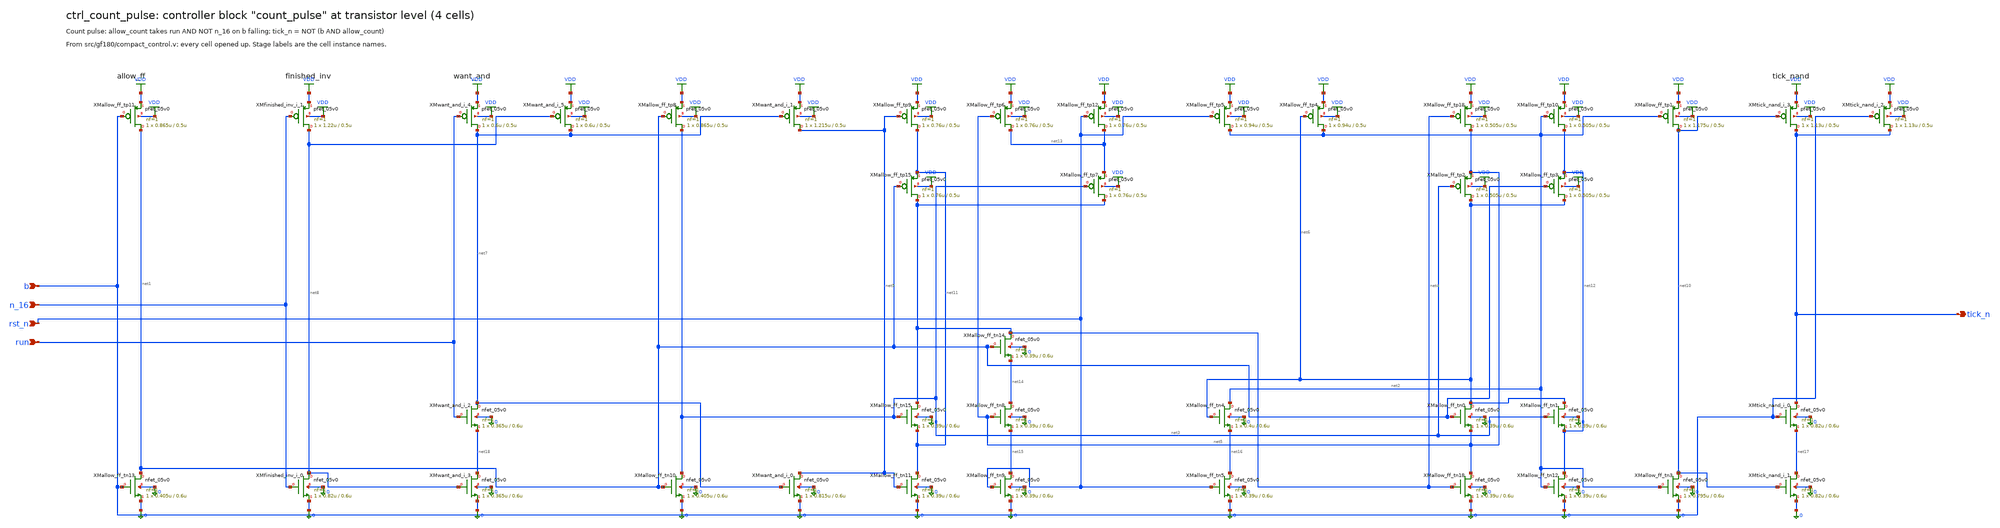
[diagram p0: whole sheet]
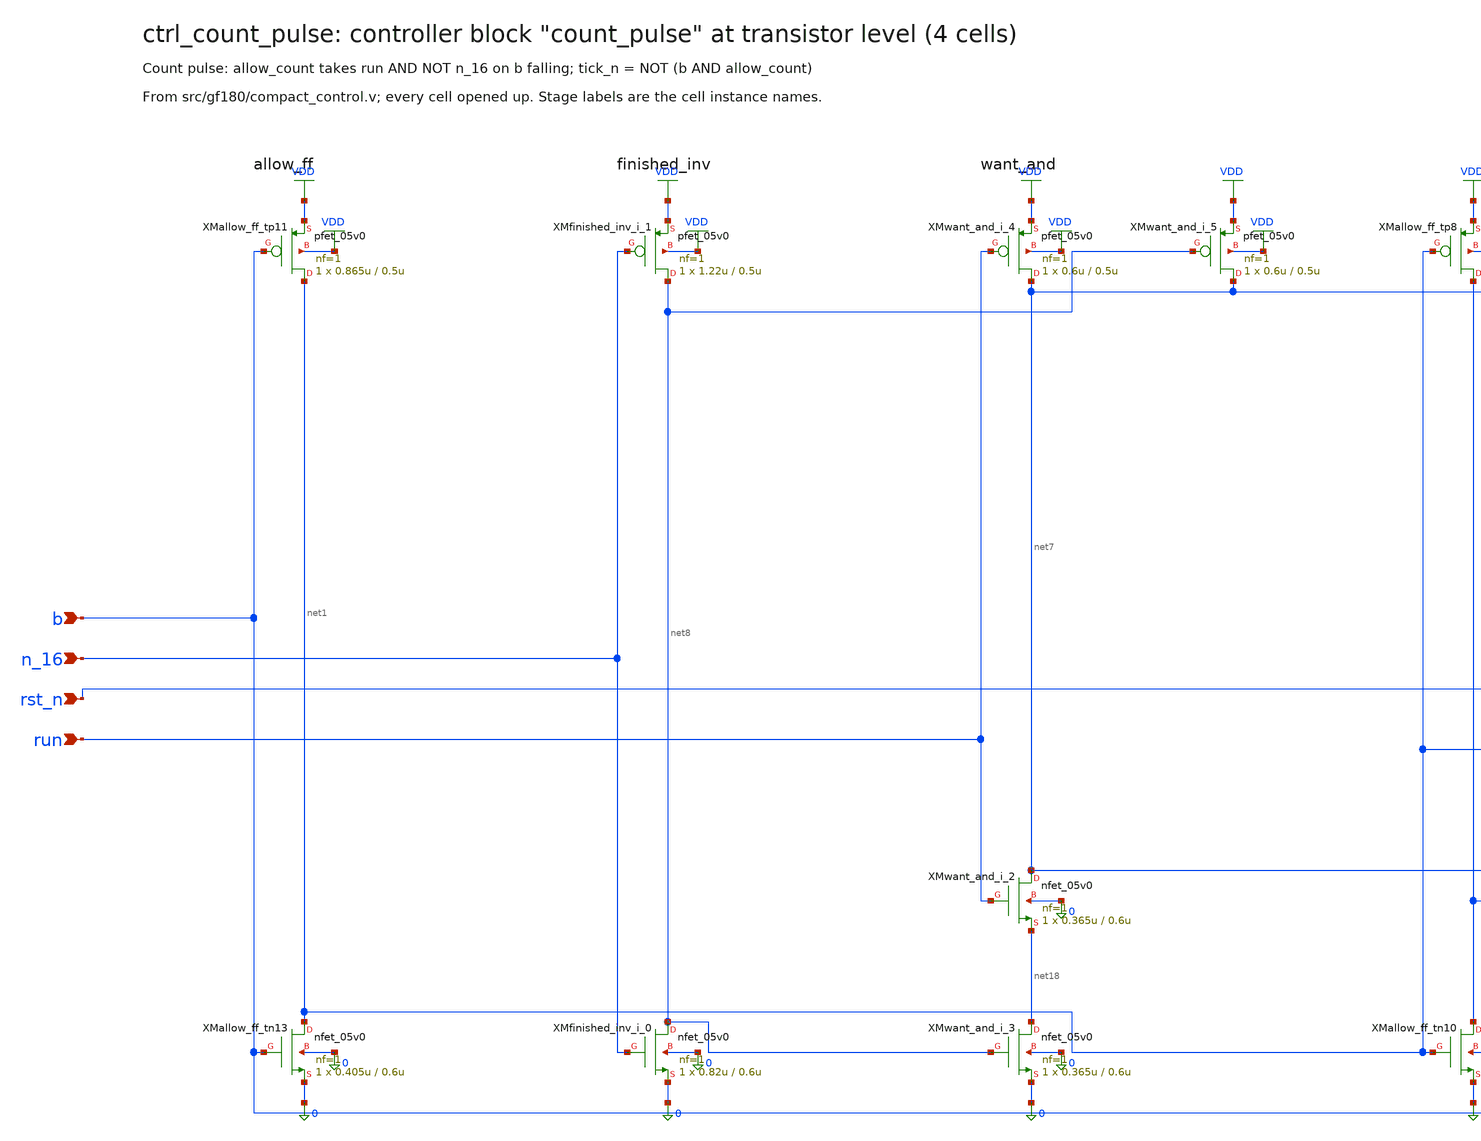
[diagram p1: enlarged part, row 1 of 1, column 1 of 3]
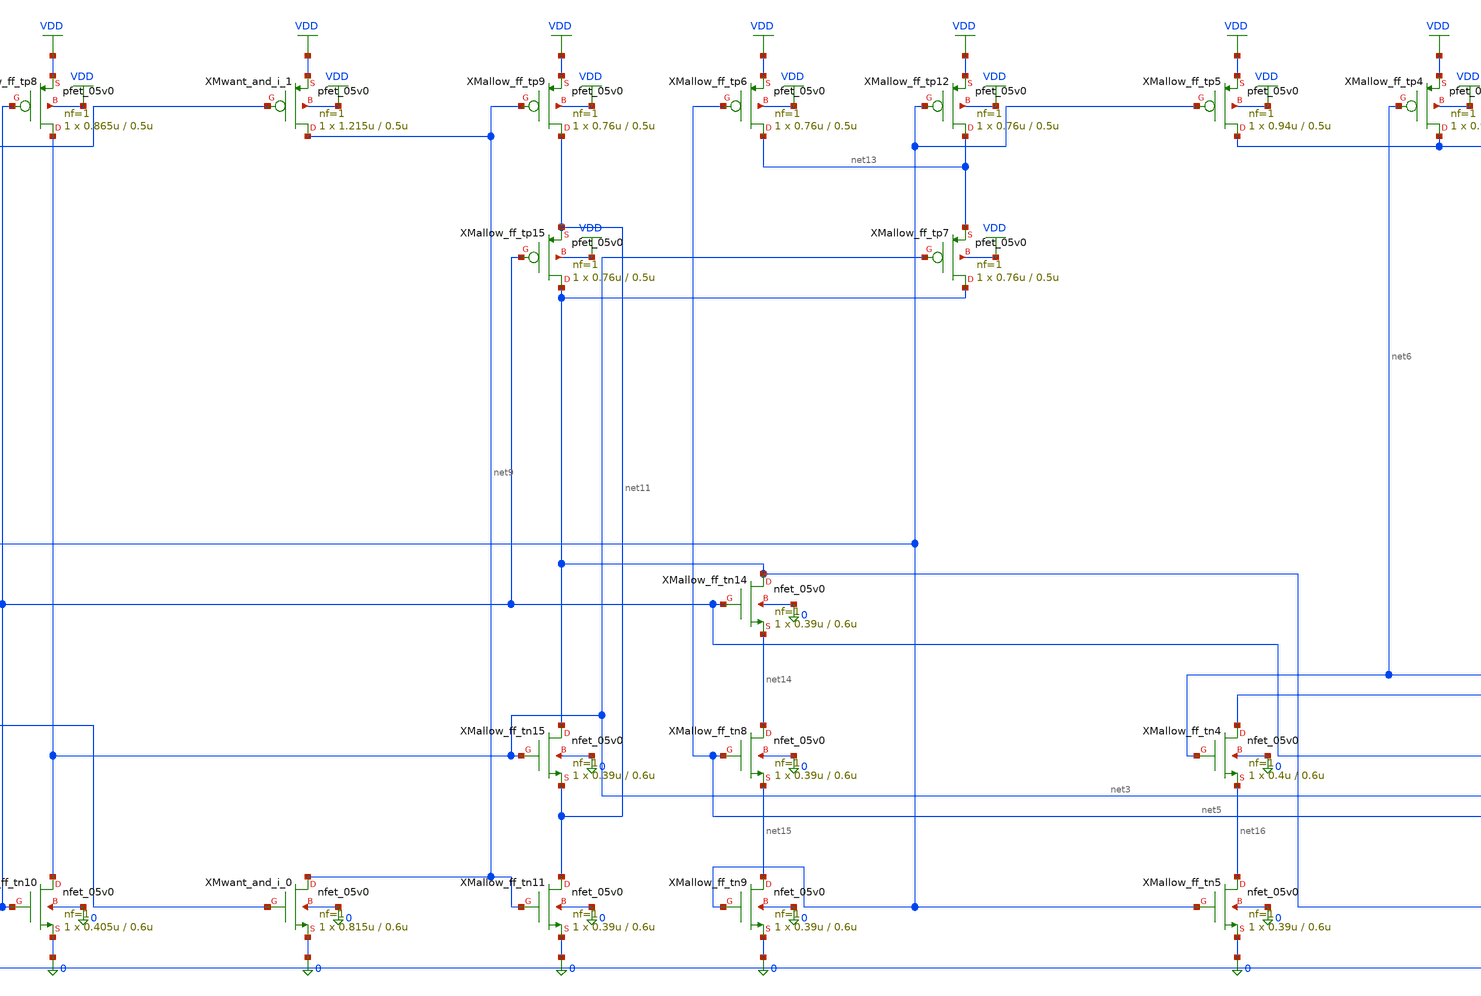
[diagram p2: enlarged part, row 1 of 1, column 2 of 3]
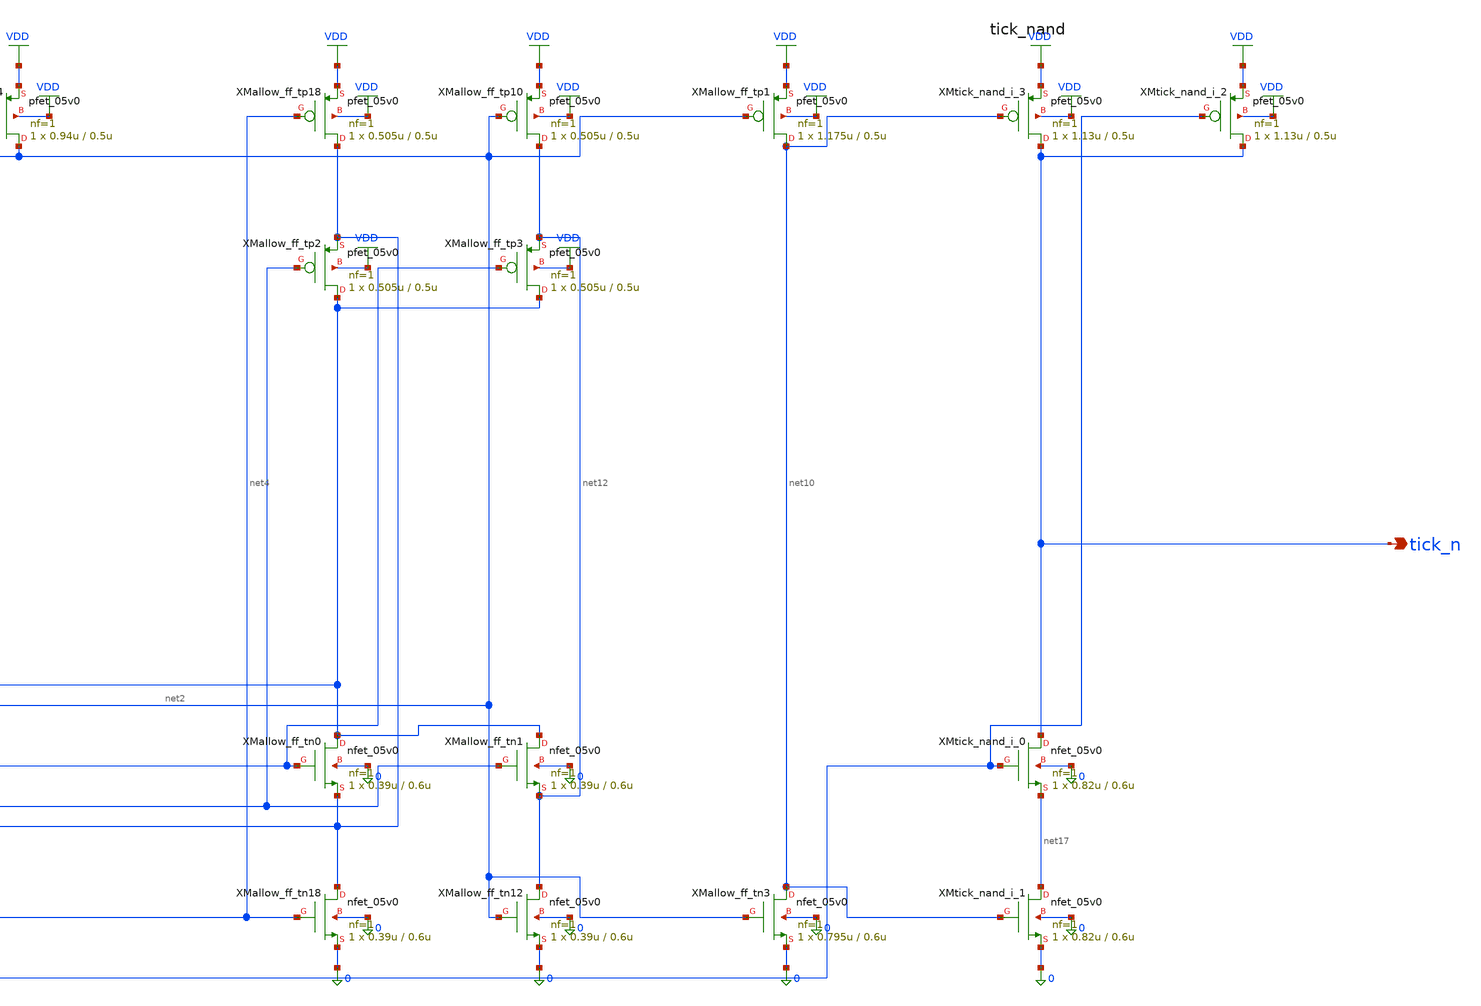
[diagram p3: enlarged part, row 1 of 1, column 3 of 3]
** sch_path: xschem/flat/ctrl_count_pulse.sch
**.subckt ctrl_count_pulse b n_16 rst_n run tick_n
*.ipin b
*.ipin n_16
*.ipin rst_n
*.ipin run
*.opin tick_n
XMallow_ff_tn13 net1 b 0 0 nfet_05v0 L=0.6u W=0.405u nf=1 ad=2.025e-13 as=2.025e-13 pd=1.81e-06
+ ps=1.81e-06 nrd=0 nrs=0 sa=0 sb=0 sd=0 m=1
XMallow_ff_tn10 net3 net1 0 0 nfet_05v0 L=0.6u W=0.405u nf=1 ad=2.025e-13 as=2.025e-13 pd=1.81e-06
+ ps=1.81e-06 nrd=0 nrs=0 sa=0 sb=0 sd=0 m=1
XMallow_ff_tn11 net11 net9 0 0 nfet_05v0 L=0.6u W=0.39u nf=1 ad=1.95e-13 as=1.95e-13 pd=1.78e-06
+ ps=1.78e-06 nrd=0 nrs=0 sa=0 sb=0 sd=0 m=1
XMallow_ff_tn15 net4 net3 net11 0 nfet_05v0 L=0.6u W=0.39u nf=1 ad=1.95e-13 as=1.95e-13 pd=1.78e-06
+ ps=1.78e-06 nrd=0 nrs=0 sa=0 sb=0 sd=0 m=1
XMallow_ff_tn14 net4 net1 net14 0 nfet_05v0 L=0.6u W=0.39u nf=1 ad=1.95e-13 as=1.95e-13 pd=1.78e-06
+ ps=1.78e-06 nrd=0 nrs=0 sa=0 sb=0 sd=0 m=1
XMallow_ff_tn8 net14 net5 net15 0 nfet_05v0 L=0.6u W=0.39u nf=1 ad=1.95e-13 as=1.95e-13 pd=1.78e-06
+ ps=1.78e-06 nrd=0 nrs=0 sa=0 sb=0 sd=0 m=1
XMallow_ff_tn9 net15 rst_n 0 0 nfet_05v0 L=0.6u W=0.39u nf=1 ad=1.95e-13 as=1.95e-13 pd=1.78e-06
+ ps=1.78e-06 nrd=0 nrs=0 sa=0 sb=0 sd=0 m=1
XMallow_ff_tn18 net5 net4 0 0 nfet_05v0 L=0.6u W=0.39u nf=1 ad=1.95e-13 as=1.95e-13 pd=1.78e-06
+ ps=1.78e-06 nrd=0 nrs=0 sa=0 sb=0 sd=0 m=1
XMallow_ff_tn0 net6 net1 net5 0 nfet_05v0 L=0.6u W=0.39u nf=1 ad=1.95e-13 as=1.95e-13 pd=1.78e-06
+ ps=1.78e-06 nrd=0 nrs=0 sa=0 sb=0 sd=0 m=1
XMallow_ff_tn1 net6 net3 net12 0 nfet_05v0 L=0.6u W=0.39u nf=1 ad=1.95e-13 as=1.95e-13 pd=1.78e-06
+ ps=1.78e-06 nrd=0 nrs=0 sa=0 sb=0 sd=0 m=1
XMallow_ff_tn12 net12 net2 0 0 nfet_05v0 L=0.6u W=0.39u nf=1 ad=1.95e-13 as=1.95e-13 pd=1.78e-06
+ ps=1.78e-06 nrd=0 nrs=0 sa=0 sb=0 sd=0 m=1
XMallow_ff_tn5 net16 rst_n 0 0 nfet_05v0 L=0.6u W=0.39u nf=1 ad=1.95e-13 as=1.95e-13 pd=1.78e-06
+ ps=1.78e-06 nrd=0 nrs=0 sa=0 sb=0 sd=0 m=1
XMallow_ff_tn4 net2 net6 net16 0 nfet_05v0 L=0.6u W=0.4u nf=1 ad=2e-13 as=2e-13 pd=1.8e-06
+ ps=1.8e-06 nrd=0 nrs=0 sa=0 sb=0 sd=0 m=1
XMallow_ff_tn3 net10 net2 0 0 nfet_05v0 L=0.6u W=0.795u nf=1 ad=3.975e-13 as=3.975e-13 pd=2.59e-06
+ ps=2.59e-06 nrd=0 nrs=0 sa=0 sb=0 sd=0 m=1
XMallow_ff_tp11 net1 b VDD VDD pfet_05v0 L=0.5u W=0.865u nf=1 ad=4.325e-13 as=4.325e-13 pd=2.73e-06
+ ps=2.73e-06 nrd=0 nrs=0 sa=0 sb=0 sd=0 m=1
XMallow_ff_tp8 net3 net1 VDD VDD pfet_05v0 L=0.5u W=0.865u nf=1 ad=4.325e-13 as=4.325e-13
+ pd=2.73e-06 ps=2.73e-06 nrd=0 nrs=0 sa=0 sb=0 sd=0 m=1
XMallow_ff_tp9 net11 net9 VDD VDD pfet_05v0 L=0.5u W=0.76u nf=1 ad=3.8e-13 as=3.8e-13 pd=2.52e-06
+ ps=2.52e-06 nrd=0 nrs=0 sa=0 sb=0 sd=0 m=1
XMallow_ff_tp15 net4 net1 net11 VDD pfet_05v0 L=0.5u W=0.76u nf=1 ad=3.8e-13 as=3.8e-13 pd=2.52e-06
+ ps=2.52e-06 nrd=0 nrs=0 sa=0 sb=0 sd=0 m=1
XMallow_ff_tp7 net4 net3 net13 VDD pfet_05v0 L=0.5u W=0.76u nf=1 ad=3.8e-13 as=3.8e-13 pd=2.52e-06
+ ps=2.52e-06 nrd=0 nrs=0 sa=0 sb=0 sd=0 m=1
XMallow_ff_tp6 net13 net5 VDD VDD pfet_05v0 L=0.5u W=0.76u nf=1 ad=3.8e-13 as=3.8e-13 pd=2.52e-06
+ ps=2.52e-06 nrd=0 nrs=0 sa=0 sb=0 sd=0 m=1
XMallow_ff_tp12 net13 rst_n VDD VDD pfet_05v0 L=0.5u W=0.76u nf=1 ad=3.8e-13 as=3.8e-13 pd=2.52e-06
+ ps=2.52e-06 nrd=0 nrs=0 sa=0 sb=0 sd=0 m=1
XMallow_ff_tp18 net5 net4 VDD VDD pfet_05v0 L=0.5u W=0.505u nf=1 ad=2.525e-13 as=2.525e-13
+ pd=2.01e-06 ps=2.01e-06 nrd=0 nrs=0 sa=0 sb=0 sd=0 m=1
XMallow_ff_tp2 net6 net3 net5 VDD pfet_05v0 L=0.5u W=0.505u nf=1 ad=2.525e-13 as=2.525e-13
+ pd=2.01e-06 ps=2.01e-06 nrd=0 nrs=0 sa=0 sb=0 sd=0 m=1
XMallow_ff_tp3 net6 net1 net12 VDD pfet_05v0 L=0.5u W=0.505u nf=1 ad=2.525e-13 as=2.525e-13
+ pd=2.01e-06 ps=2.01e-06 nrd=0 nrs=0 sa=0 sb=0 sd=0 m=1
XMallow_ff_tp10 net12 net2 VDD VDD pfet_05v0 L=0.5u W=0.505u nf=1 ad=2.525e-13 as=2.525e-13
+ pd=2.01e-06 ps=2.01e-06 nrd=0 nrs=0 sa=0 sb=0 sd=0 m=1
XMallow_ff_tp5 net2 rst_n VDD VDD pfet_05v0 L=0.5u W=0.94u nf=1 ad=4.7e-13 as=4.7e-13 pd=2.88e-06
+ ps=2.88e-06 nrd=0 nrs=0 sa=0 sb=0 sd=0 m=1
XMallow_ff_tp4 net2 net6 VDD VDD pfet_05v0 L=0.5u W=0.94u nf=1 ad=4.7e-13 as=4.7e-13 pd=2.88e-06
+ ps=2.88e-06 nrd=0 nrs=0 sa=0 sb=0 sd=0 m=1
XMallow_ff_tp1 net10 net2 VDD VDD pfet_05v0 L=0.5u W=1.175u nf=1 ad=5.875e-13 as=5.875e-13
+ pd=3.35e-06 ps=3.35e-06 nrd=0 nrs=0 sa=0 sb=0 sd=0 m=1
XMfinished_inv_i_0 net8 n_16 0 0 nfet_05v0 L=0.6u W=0.82u nf=1 ad=4.1e-13 as=4.1e-13 pd=2.64e-06
+ ps=2.64e-06 nrd=0 nrs=0 sa=0 sb=0 sd=0 m=1
XMfinished_inv_i_1 net8 n_16 VDD VDD pfet_05v0 L=0.5u W=1.22u nf=1 ad=6.1e-13 as=6.1e-13 pd=3.44e-06
+ ps=3.44e-06 nrd=0 nrs=0 sa=0 sb=0 sd=0 m=1
XMtick_nand_i_1 net17 net10 0 0 nfet_05v0 L=0.6u W=0.82u nf=1 ad=4.1e-13 as=4.1e-13 pd=2.64e-06
+ ps=2.64e-06 nrd=0 nrs=0 sa=0 sb=0 sd=0 m=1
XMtick_nand_i_0 tick_n b net17 0 nfet_05v0 L=0.6u W=0.82u nf=1 ad=4.1e-13 as=4.1e-13 pd=2.64e-06
+ ps=2.64e-06 nrd=0 nrs=0 sa=0 sb=0 sd=0 m=1
XMtick_nand_i_3 tick_n net10 VDD VDD pfet_05v0 L=0.5u W=1.13u nf=1 ad=5.65e-13 as=5.65e-13
+ pd=3.26e-06 ps=3.26e-06 nrd=0 nrs=0 sa=0 sb=0 sd=0 m=1
XMtick_nand_i_2 tick_n b VDD VDD pfet_05v0 L=0.5u W=1.13u nf=1 ad=5.65e-13 as=5.65e-13 pd=3.26e-06
+ ps=3.26e-06 nrd=0 nrs=0 sa=0 sb=0 sd=0 m=1
XMwant_and_i_2 net7 run net18 0 nfet_05v0 L=0.6u W=0.365u nf=1 ad=1.825e-13 as=1.825e-13 pd=1.73e-06
+ ps=1.73e-06 nrd=0 nrs=0 sa=0 sb=0 sd=0 m=1
XMwant_and_i_3 net18 net8 0 0 nfet_05v0 L=0.6u W=0.365u nf=1 ad=1.825e-13 as=1.825e-13 pd=1.73e-06
+ ps=1.73e-06 nrd=0 nrs=0 sa=0 sb=0 sd=0 m=1
XMwant_and_i_0 net9 net7 0 0 nfet_05v0 L=0.6u W=0.815u nf=1 ad=4.075e-13 as=4.075e-13 pd=2.63e-06
+ ps=2.63e-06 nrd=0 nrs=0 sa=0 sb=0 sd=0 m=1
XMwant_and_i_4 net7 run VDD VDD pfet_05v0 L=0.5u W=0.6u nf=1 ad=3e-13 as=3e-13 pd=2.2e-06 ps=2.2e-06
+ nrd=0 nrs=0 sa=0 sb=0 sd=0 m=1
XMwant_and_i_5 net7 net8 VDD VDD pfet_05v0 L=0.5u W=0.6u nf=1 ad=3e-13 as=3e-13 pd=2.2e-06
+ ps=2.2e-06 nrd=0 nrs=0 sa=0 sb=0 sd=0 m=1
XMwant_and_i_1 net9 net7 VDD VDD pfet_05v0 L=0.5u W=1.215u nf=1 ad=6.075e-13 as=6.075e-13
+ pd=3.43e-06 ps=3.43e-06 nrd=0 nrs=0 sa=0 sb=0 sd=0 m=1
**.ends
.GLOBAL VDD
.end
